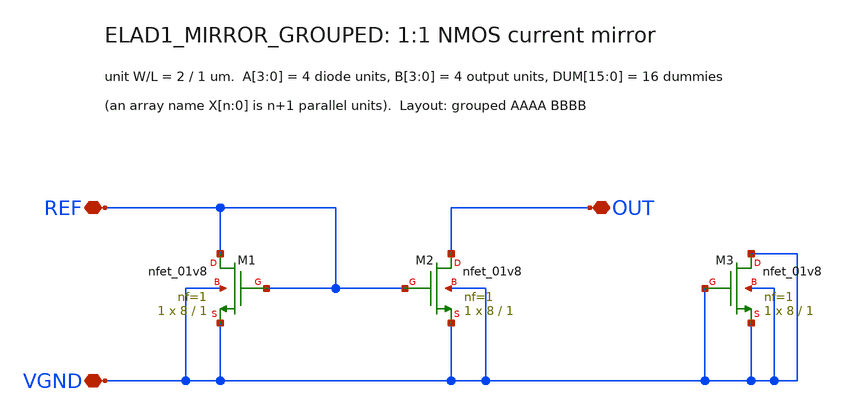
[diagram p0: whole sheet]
** sch_path: cells/ELAD1_MIRROR_GROUPED/schematic/ELAD1_MIRROR_GROUPED.sch
**.subckt ELAD1_MIRROR_GROUPED REF OUT VGND
*.iopin REF
*.iopin OUT
*.iopin VGND
XM1 REF REF VGND VGND sky130_fd_pr__nfet_01v8 L=1 W=8 nf=1 ad='int((1 + 1)/2) * 8 / 1 * 0.29' as='int((1 + 2)/2) * 8 / 1 * 0.29'
+ pd='2*int((1 + 1)/2) * (8 / 1 + 0.29)' ps='2*int((1 + 2)/2) * (8 / 1 + 0.29)' nrd='0.29 / 8 ' nrs='0.29 / 8 '
+ sa=0 sb=0 sd=0 mult=1 m=1
XM2 OUT REF VGND VGND sky130_fd_pr__nfet_01v8 L=1 W=8 nf=1 ad='int((1 + 1)/2) * 8 / 1 * 0.29' as='int((1 + 2)/2) * 8 / 1 * 0.29'
+ pd='2*int((1 + 1)/2) * (8 / 1 + 0.29)' ps='2*int((1 + 2)/2) * (8 / 1 + 0.29)' nrd='0.29 / 8 ' nrs='0.29 / 8 '
+ sa=0 sb=0 sd=0 mult=1 m=1
XM3 VGND VGND VGND VGND sky130_fd_pr__nfet_01v8 L=1 W=8 nf=1 ad='int((1 + 1)/2) * 8 / 1 * 0.29' as='int((1 + 2)/2) * 8 / 1 * 0.29'
+ pd='2*int((1 + 1)/2) * (8 / 1 + 0.29)' ps='2*int((1 + 2)/2) * (8 / 1 + 0.29)' nrd='0.29 / 8 ' nrs='0.29 / 8 '
+ sa=0 sb=0 sd=0 mult=1 m=1
**.ends
.end
